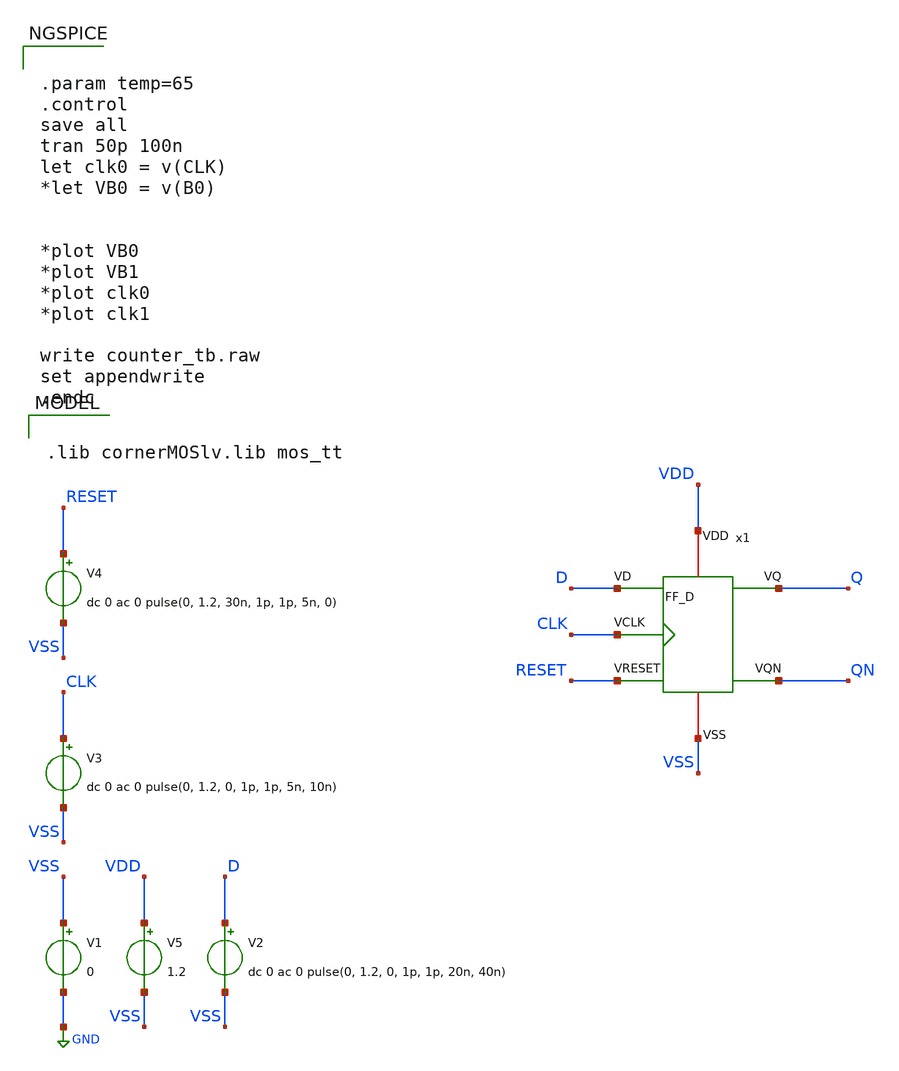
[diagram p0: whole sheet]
** sch_path: W2WDAC_Project/GROTDC/GROTDC_SIM/tb_FF_D.sch
**.subckt tb_FF_D
x1 VDD CLK RESET VSS Q QN D FF_D
V1 VSS GND 0
V3 CLK VSS dc 0 ac 0 pulse(0, 1.2, 0, 1p, 1p, 5n, 10n)
V5 VDD VSS 1.2
V4 RESET VSS dc 0 ac 0 pulse(0, 1.2, 30n, 1p, 1p, 5n, 0)
V2 D VSS dc 0 ac 0 pulse(0, 1.2, 0, 1p, 1p, 20n, 40n)
**** begin user architecture code


.param temp=65
.control
save all
tran 50p 100n
let clk0 = v(CLK)
*let VB0 = v(B0)


*plot VB0
*plot VB1
*plot clk0
*plot clk1

write counter_tb.raw
set appendwrite
.endc



.lib cornerMOSlv.lib mos_tt

**** end user architecture code
**.ends
.GLOBAL GND
.end
